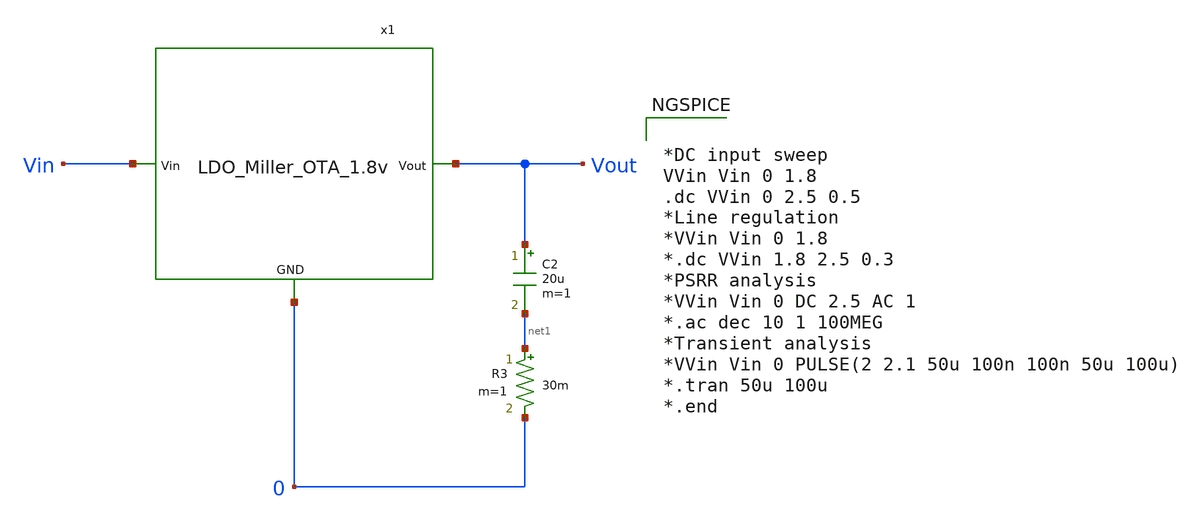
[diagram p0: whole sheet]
** sch_path: Analog_Blocks/LDO/Testbench/LDO_Miller_1.8v_TB.sch
**.subckt LDO_Miller_1.8v_TB
C2 Vout net1 20u m=1
R3 net1 0 30m m=1
x1 Vin Vout 0 LDO_Miller_OTA_1.8v
**** begin user architecture code

.include $::SKYWATER_MODELS/cells/nfet_01v8/sky130_fd_pr__nfet_01v8__tt.corner.spice
.include $::SKYWATER_MODELS/cells/nfet_01v8_lvt/sky130_fd_pr__nfet_01v8_lvt__tt.corner.spice
.include $::SKYWATER_MODELS/cells/pfet_01v8/sky130_fd_pr__pfet_01v8__tt.corner.spice
.include $::SKYWATER_MODELS/cells/nfet_03v3_nvt/sky130_fd_pr__nfet_03v3_nvt__tt.corner.spice
.include $::SKYWATER_MODELS/cells/nfet_05v0_nvt/sky130_fd_pr__nfet_05v0_nvt__tt.corner.spice
.include $::SKYWATER_MODELS/cells/esd_nfet_01v8/sky130_fd_pr__esd_nfet_01v8__tt.corner.spice
.include $::SKYWATER_MODELS/cells/pfet_01v8_lvt/sky130_fd_pr__pfet_01v8_lvt__tt.corner.spice
.include $::SKYWATER_MODELS/cells/pfet_01v8_hvt/sky130_fd_pr__pfet_01v8_hvt__tt.corner.spice
.include $::SKYWATER_MODELS/cells/esd_pfet_g5v0d10v5/sky130_fd_pr__esd_pfet_g5v0d10v5__tt.corner.spice
.include $::SKYWATER_MODELS/cells/pfet_g5v0d10v5/sky130_fd_pr__pfet_g5v0d10v5__tt.corner.spice
.include $::SKYWATER_MODELS/cells/pfet_g5v0d16v0/sky130_fd_pr__pfet_g5v0d16v0__tt.corner.spice
.include $::SKYWATER_MODELS/cells/nfet_g5v0d10v5/sky130_fd_pr__nfet_g5v0d10v5__tt.corner.spice
.include $::SKYWATER_MODELS/cells/nfet_g5v0d16v0/sky130_fd_pr__nfet_g5v0d16v0__tt_discrete.corner.spice
.include $::SKYWATER_MODELS/cells/esd_nfet_g5v0d10v5/sky130_fd_pr__esd_nfet_g5v0d10v5__tt.corner.spice
.include $::SKYWATER_MODELS/models/corners/tt/nonfet.spice
* Mismatch parameters
.include $::SKYWATER_MODELS/cells/nfet_01v8/sky130_fd_pr__nfet_01v8__mismatch.corner.spice
.include $::SKYWATER_MODELS/cells/pfet_01v8/sky130_fd_pr__pfet_01v8__mismatch.corner.spice
.include $::SKYWATER_MODELS/cells/nfet_01v8_lvt/sky130_fd_pr__nfet_01v8_lvt__mismatch.corner.spice
.include $::SKYWATER_MODELS/cells/pfet_01v8_lvt/sky130_fd_pr__pfet_01v8_lvt__mismatch.corner.spice
.include $::SKYWATER_MODELS/cells/pfet_01v8_hvt/sky130_fd_pr__pfet_01v8_hvt__mismatch.corner.spice
.include $::SKYWATER_MODELS/cells/nfet_g5v0d10v5/sky130_fd_pr__nfet_g5v0d10v5__mismatch.corner.spice
.include $::SKYWATER_MODELS/cells/pfet_g5v0d10v5/sky130_fd_pr__pfet_g5v0d10v5__mismatch.corner.spice
.include $::SKYWATER_MODELS/cells/nfet_05v0_nvt/sky130_fd_pr__nfet_05v0_nvt__mismatch.corner.spice
.include $::SKYWATER_MODELS/cells/nfet_03v3_nvt/sky130_fd_pr__nfet_03v3_nvt__mismatch.corner.spice
* Resistor$::SKYWATER_MODELS/Capacitor
.include $::SKYWATER_MODELS/models/r+c/res_typical__cap_typical.spice
.include $::SKYWATER_MODELS/models/r+c/res_typical__cap_typical__lin.spice
* Special cells
.include $::SKYWATER_MODELS/models/corners/tt/specialized_cells.spice
* All models
.include $::SKYWATER_MODELS/models/all.spice
* Corner
.include $::SKYWATER_MODELS/models/corners/tt/rf.spice



*DC input sweep
VVin Vin 0 1.8
.dc VVin 0 2.5 0.5
*Line regulation
*VVin Vin 0 1.8
*.dc VVin 1.8 2.5 0.3
*PSRR analysis
*VVin Vin 0 DC 2.5 AC 1
*.ac dec 10 1 100MEG
*Transient analysis
*VVin Vin 0 PULSE(2 2.1 50u 100n 100n 50u 100u)
*.tran 50u 100u
*.end


**** end user architecture code
**.ends
.end
